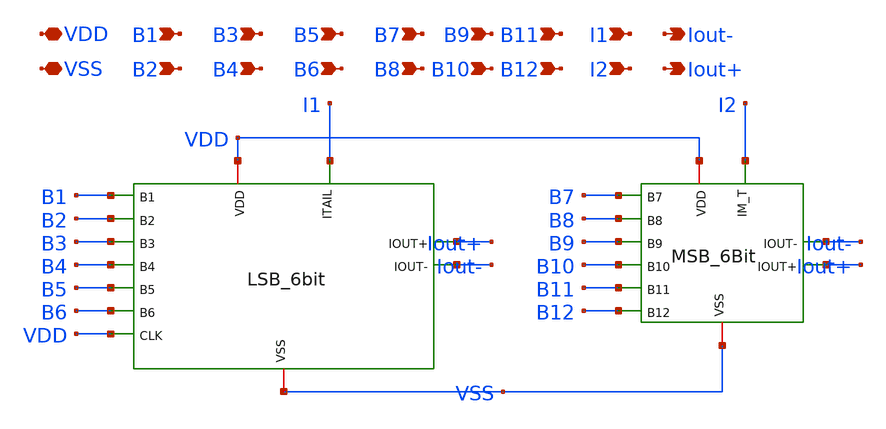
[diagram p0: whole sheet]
** sch_path: DAC_PAKISTAN_01/Pakistan1_Xschem/DAC_12Bit_V2.sch
**.subckt DAC_12Bit_V2 VDD VSS B1 B2 B3 B4 B5 B6 B7 B8 B9 B10 B11 B12 I1 I2 Iout- Iout+
*.iopin VDD
*.iopin VSS
*.ipin B1
*.ipin B2
*.ipin B3
*.ipin B4
*.ipin B5
*.ipin B6
*.ipin B7
*.ipin B8
*.ipin B9
*.ipin B10
*.ipin B11
*.ipin B12
*.ipin I1
*.ipin I2
*.opin Iout-
*.opin Iout+
x1 VDD VSS B1 B2 B3 B4 B5 B6 VDD I1 Iout+ Iout- LSB
x3 VSS VDD B11 B7 B8 B12 B9 I2 B10 Iout- Iout+ MSB_6Bit
**.ends
.end
